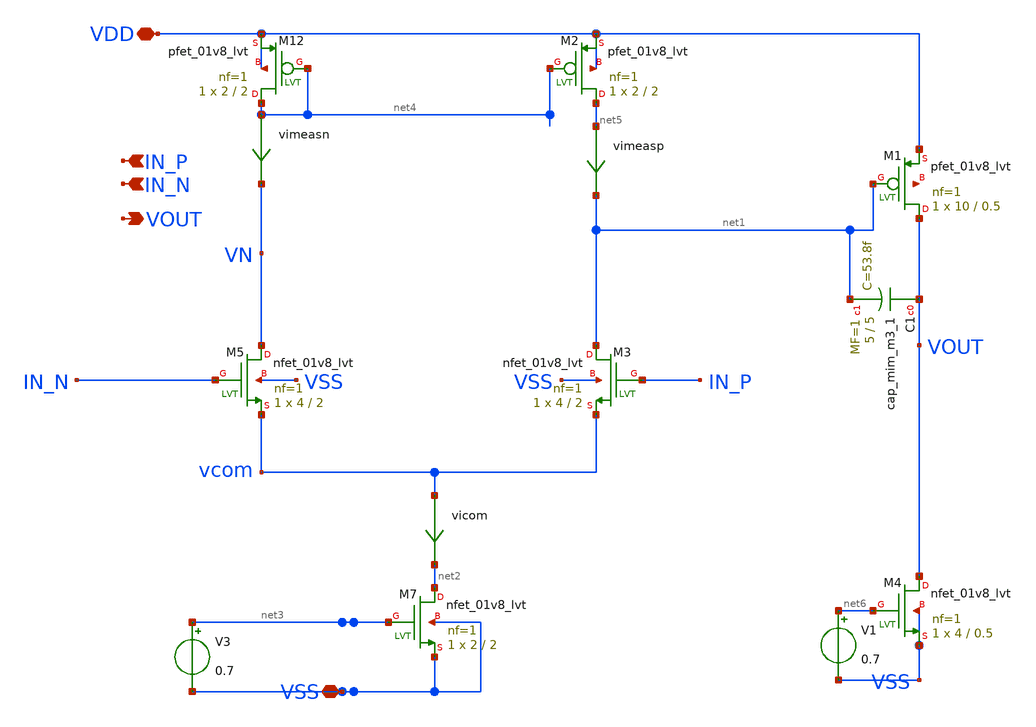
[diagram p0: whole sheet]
** sch_path: xschem/opamp3.sch
**.subckt opamp3 VDD VSS IN_N VOUT IN_P
*.iopin VDD
*.iopin VSS
*.ipin IN_N
*.opin VOUT
*.ipin IN_P
vimeasn net4 VN 0
.save i(vimeasn)
vimeasp net5 net1 0
.save i(vimeasp)
vicom vcom net2 0
.save i(vicom)
XM7 net2 net3 VSS VSS sky130_fd_pr__nfet_01v8_lvt L=2 W=2 nf=1 ad='int((nf+1)/2) * W/nf * 0.29' as='int((nf+2)/2) * W/nf * 0.29'
+ pd='2*int((nf+1)/2) * (W/nf + 0.29)' ps='2*int((nf+2)/2) * (W/nf + 0.29)' nrd='0.29 / W' nrs='0.29 / W'
+ sa=0 sb=0 sd=0 mult=1 m=1
XM12 net4 net4 VDD VDD sky130_fd_pr__pfet_01v8_lvt L=2 W=2 nf=1 ad='int((nf+1)/2) * W/nf * 0.29' as='int((nf+2)/2) * W/nf * 0.29'
+ pd='2*int((nf+1)/2) * (W/nf + 0.29)' ps='2*int((nf+2)/2) * (W/nf + 0.29)' nrd='0.29 / W' nrs='0.29 / W'
+ sa=0 sb=0 sd=0 mult=1 m=1
XM2 net5 net4 VDD VDD sky130_fd_pr__pfet_01v8_lvt L=2 W=2 nf=1 ad='int((nf+1)/2) * W/nf * 0.29' as='int((nf+2)/2) * W/nf * 0.29'
+ pd='2*int((nf+1)/2) * (W/nf + 0.29)' ps='2*int((nf+2)/2) * (W/nf + 0.29)' nrd='0.29 / W' nrs='0.29 / W'
+ sa=0 sb=0 sd=0 mult=1 m=1
XM3 net1 IN_P vcom VSS sky130_fd_pr__nfet_01v8_lvt L=2 W=4 nf=1 ad='int((nf+1)/2) * W/nf * 0.29' as='int((nf+2)/2) * W/nf * 0.29'
+ pd='2*int((nf+1)/2) * (W/nf + 0.29)' ps='2*int((nf+2)/2) * (W/nf + 0.29)' nrd='0.29 / W' nrs='0.29 / W'
+ sa=0 sb=0 sd=0 mult=1 m=1
XM5 VN IN_N vcom VSS sky130_fd_pr__nfet_01v8_lvt L=2 W=4 nf=1 ad='int((nf+1)/2) * W/nf * 0.29' as='int((nf+2)/2) * W/nf * 0.29'
+ pd='2*int((nf+1)/2) * (W/nf + 0.29)' ps='2*int((nf+2)/2) * (W/nf + 0.29)' nrd='0.29 / W' nrs='0.29 / W'
+ sa=0 sb=0 sd=0 mult=1 m=1
V3 net3 VSS 0.7
XM1 VOUT net1 VDD net7 sky130_fd_pr__pfet_01v8_lvt L=0.5 W=10 nf=1 ad='int((nf+1)/2) * W/nf * 0.29' as='int((nf+2)/2) * W/nf * 0.29'
+ pd='2*int((nf+1)/2) * (W/nf + 0.29)' ps='2*int((nf+2)/2) * (W/nf + 0.29)' nrd='0.29 / W' nrs='0.29 / W'
+ sa=0 sb=0 sd=0 mult=1 m=1
XM4 VOUT net6 VSS VSS sky130_fd_pr__nfet_01v8_lvt L=0.5 W=4 nf=1 ad='int((nf+1)/2) * W/nf * 0.29' as='int((nf+2)/2) * W/nf * 0.29'
+ pd='2*int((nf+1)/2) * (W/nf + 0.29)' ps='2*int((nf+2)/2) * (W/nf + 0.29)' nrd='0.29 / W' nrs='0.29 / W'
+ sa=0 sb=0 sd=0 mult=1 m=1
V1 net6 VSS 0.7
XC1 VOUT net1 sky130_fd_pr__cap_mim_m3_1 W=5 L=5 MF=1 m=1
**.ends
.end
